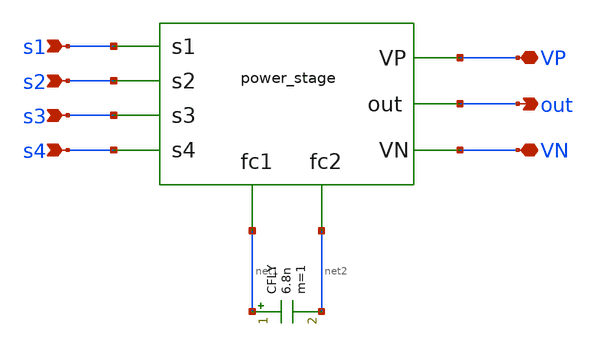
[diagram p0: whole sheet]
** sch_path: xschem/release/converter.sch
**.subckt converter s1 s2 s3 s4 VP VN out
*.ipin s1
*.ipin s2
*.ipin s3
*.ipin s4
*.iopin VP
*.iopin VN
*.opin out
X1 s1 s2 s3 s4 net1 net2 out VP VN power_stage
CFLY net1 net2 6.8n m=1
**.ends
.end
